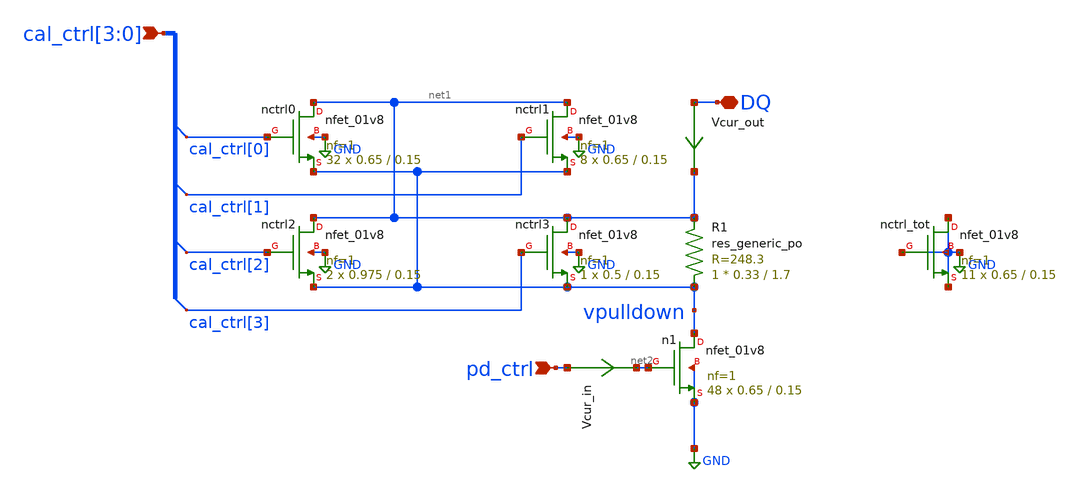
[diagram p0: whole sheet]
** sch_path: schem/n-leg.sch
* Copyright 2021 Stefan Frederik Schippers
* Licensed under the Apache License, Version 2.0 (the "License");
* you may not use this file except in compliance with the License.
* You may obtain a copy of the License at
* https://www.apache.org/licenses/LICENSE-2.0
* Unless required by applicable law or agreed to in writing, software
* distributed under the License is distributed on an "AS IS" BASIS,
* WITHOUT WARRANTIES OR CONDITIONS OF ANY KIND, either express or implied.
* See the License for the specific language governing permissions and
* limitations under the License.
**.subckt n-leg DQ pd_ctrl cal_ctrl[3],cal_ctrl[2],cal_ctrl[1],cal_ctrl[0]
*.iopin DQ
*.ipin pd_ctrl
*.ipin cal_ctrl[3],cal_ctrl[2],cal_ctrl[1],cal_ctrl[0]
XR1 vpulldown net1 sky130_fd_pr__res_generic_po W=0.33 L=1.7 m=1
Xn1 vpulldown net2 GND GND sky130_fd_pr__nfet_01v8 L=0.15 W=0.65 nf=1 ad='int((nf+1)/2) * W/nf * 0.29'
+ as='int((nf+2)/2) * W/nf * 0.29' pd='2*int((nf+1)/2) * (W/nf + 0.29)' ps='2*int((nf+2)/2) * (W/nf + 0.29)'
+ nrd='0.29 / W' nrs='0.29 / W' sa=0 sb=0 sd=0 mult=48 m=48
Xnctrl0 net1 cal_ctrl[0] vpulldown GND sky130_fd_pr__nfet_01v8 L=0.15 W=0.65 nf=1 ad='int((nf+1)/2) * W/nf * 0.29'
+ as='int((nf+2)/2) * W/nf * 0.29' pd='2*int((nf+1)/2) * (W/nf + 0.29)' ps='2*int((nf+2)/2) * (W/nf + 0.29)'
+ nrd='0.29 / W' nrs='0.29 / W' sa=0 sb=0 sd=0 mult=32 m=32
Xnctrl1 net1 cal_ctrl[1] vpulldown GND sky130_fd_pr__nfet_01v8 L=0.15 W=0.65 nf=1 ad='int((nf+1)/2) * W/nf * 0.29'
+ as='int((nf+2)/2) * W/nf * 0.29' pd='2*int((nf+1)/2) * (W/nf + 0.29)' ps='2*int((nf+2)/2) * (W/nf + 0.29)'
+ nrd='0.29 / W' nrs='0.29 / W' sa=0 sb=0 sd=0 mult=8 m=8
Xnctrl2 net1 cal_ctrl[2] vpulldown GND sky130_fd_pr__nfet_01v8 L=0.15 W=0.975 nf=1 ad='int((nf+1)/2) * W/nf * 0.29'
+ as='int((nf+2)/2) * W/nf * 0.29' pd='2*int((nf+1)/2) * (W/nf + 0.29)' ps='2*int((nf+2)/2) * (W/nf + 0.29)'
+ nrd='0.29 / W' nrs='0.29 / W' sa=0 sb=0 sd=0 mult=2 m=2
Xnctrl3 net1 cal_ctrl[3] vpulldown GND sky130_fd_pr__nfet_01v8 L=0.15 W=0.5 nf=1 ad='int((nf+1)/2) * W/nf * 0.29'
+ as='int((nf+2)/2) * W/nf * 0.29' pd='2*int((nf+1)/2) * (W/nf + 0.29)' ps='2*int((nf+2)/2) * (W/nf + 0.29)'
+ nrd='0.29 / W' nrs='0.29 / W' sa=0 sb=0 sd=0 mult=1 m=1
Xnctrl_tot GND GND GND GND sky130_fd_pr__nfet_01v8 L=0.15 W=0.65 nf=1 ad='int((nf+1)/2) * W/nf * 0.29'
+ as='int((nf+2)/2) * W/nf * 0.29' pd='2*int((nf+1)/2) * (W/nf + 0.29)' ps='2*int((nf+2)/2) * (W/nf + 0.29)'
+ nrd='0.29 / W' nrs='0.29 / W' sa=0 sb=0 sd=0 mult=11 m=11
Vcur_out DQ net1 0
.save i(vcur_out)
Vcur_in pd_ctrl net2 0
.save i(vcur_in)
**.ends
.GLOBAL GND
.end
